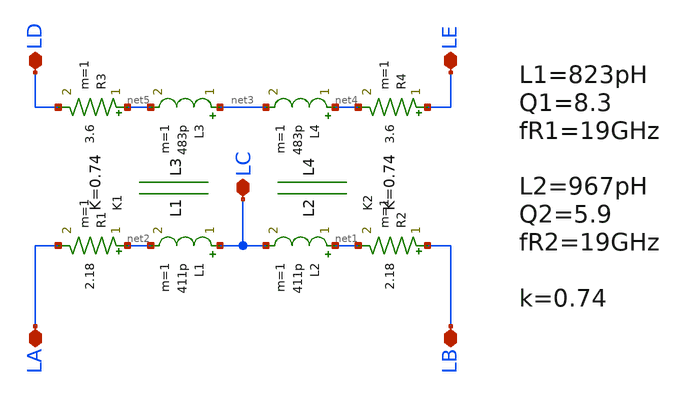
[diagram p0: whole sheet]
** sch_path: xschem/iruwbtx7_balun.sch
**.subckt iruwbtx7_balun LC LA LB LD LE
*.iopin LC
*.iopin LA
*.iopin LB
*.iopin LD
*.iopin LE
L1 LC net2 411p m=1
L2 net1 LC 411p m=1
R1 net2 LA 2.18 m=1
R2 LB net1 2.18 m=1
L3 net3 net5 483p m=1
L4 net4 net3 483p m=1
R3 net5 LD 3.6 m=1
R4 LE net4 3.6 m=1
K1 L1 L3 0.74
K2 L2 L4 0.74
**.ends
.end
